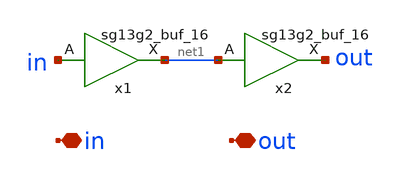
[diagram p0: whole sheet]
** sch_path: clock_gen_cycle/buffer.sch
**.subckt buffer in out
*.iopin in
*.iopin out
x1 net1 in VDD VSS sg13g2_buf_16
x2 out net1 VDD VSS sg13g2_buf_16
**.ends

* expanding   symbol:  sg13g2_stdcells/sg13g2_buf_16.sym # of pins=2
** sym_path: sg13g2_stdcells/sg13g2_buf_16.sym
** sch_path: sg13g2_stdcells/sg13g2_buf_16.sch
.subckt sg13g2_buf_16 X A VDD VSS
*.ipin A
*.opin X
*.iopin VDD
*.iopin VSS
XM1 net1 A VSS VSS sg13_lv_nmos w=4.44u l=130.00n ng=6 m=1 mm_ok=1
XM2 X net1 VSS VSS sg13_lv_nmos w=11.84u l=130.00n ng=16 m=1 mm_ok=1
XM3 net1 A VDD VDD sg13_lv_pmos w=6.72u l=130.00n ng=6 m=1 mm_ok=1
XM4 X net1 VDD VDD sg13_lv_pmos w=17.92u l=130.00n ng=16 m=1 mm_ok=1
.ends

.end
